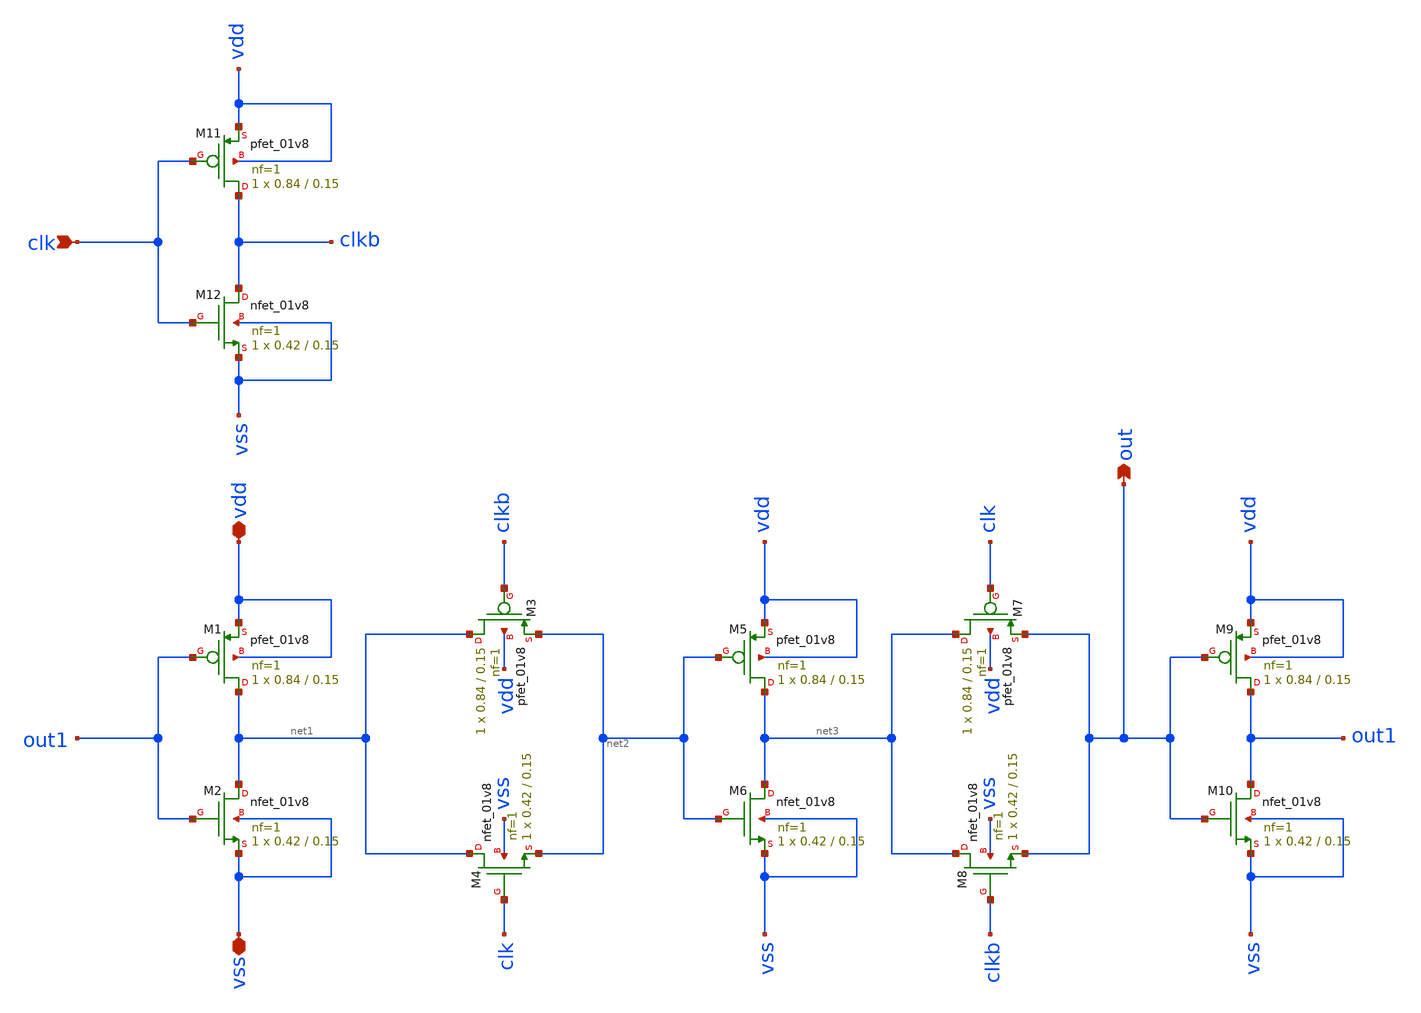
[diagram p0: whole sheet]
** sch_path: sch/PLL_caravel/FD.sch
**.subckt FD vss clk out vdd
*.iopin vss
*.ipin clk
*.opin out
*.iopin vdd
XM1 net1 out1 vdd vdd sky130_fd_pr__pfet_01v8 L=0.15 W=0.84 nf=1 ad='int((nf+1)/2) * W/nf * 0.29' as='int((nf+2)/2) * W/nf * 0.29'
+ pd='2*int((nf+1)/2) * (W/nf + 0.29)' ps='2*int((nf+2)/2) * (W/nf + 0.29)' nrd='0.29 / W' nrs='0.29 / W'
+ sa=0 sb=0 sd=0 mult=1 m=1
XM2 net1 out1 vss vss sky130_fd_pr__nfet_01v8 L=0.15 W=0.42 nf=1 ad='int((nf+1)/2) * W/nf * 0.29' as='int((nf+2)/2) * W/nf * 0.29'
+ pd='2*int((nf+1)/2) * (W/nf + 0.29)' ps='2*int((nf+2)/2) * (W/nf + 0.29)' nrd='0.29 / W' nrs='0.29 / W'
+ sa=0 sb=0 sd=0 mult=1 m=1
XM3 net1 clkb net2 vdd sky130_fd_pr__pfet_01v8 L=0.15 W=0.84 nf=1 ad='int((nf+1)/2) * W/nf * 0.29' as='int((nf+2)/2) * W/nf * 0.29'
+ pd='2*int((nf+1)/2) * (W/nf + 0.29)' ps='2*int((nf+2)/2) * (W/nf + 0.29)' nrd='0.29 / W' nrs='0.29 / W'
+ sa=0 sb=0 sd=0 mult=1 m=1
XM4 net1 clk net2 vss sky130_fd_pr__nfet_01v8 L=0.15 W=0.42 nf=1 ad='int((nf+1)/2) * W/nf * 0.29' as='int((nf+2)/2) * W/nf * 0.29'
+ pd='2*int((nf+1)/2) * (W/nf + 0.29)' ps='2*int((nf+2)/2) * (W/nf + 0.29)' nrd='0.29 / W' nrs='0.29 / W'
+ sa=0 sb=0 sd=0 mult=1 m=1
XM5 net3 net2 vdd vdd sky130_fd_pr__pfet_01v8 L=0.15 W=0.84 nf=1 ad='int((nf+1)/2) * W/nf * 0.29' as='int((nf+2)/2) * W/nf * 0.29'
+ pd='2*int((nf+1)/2) * (W/nf + 0.29)' ps='2*int((nf+2)/2) * (W/nf + 0.29)' nrd='0.29 / W' nrs='0.29 / W'
+ sa=0 sb=0 sd=0 mult=1 m=1
XM6 net3 net2 vss vss sky130_fd_pr__nfet_01v8 L=0.15 W=0.42 nf=1 ad='int((nf+1)/2) * W/nf * 0.29' as='int((nf+2)/2) * W/nf * 0.29'
+ pd='2*int((nf+1)/2) * (W/nf + 0.29)' ps='2*int((nf+2)/2) * (W/nf + 0.29)' nrd='0.29 / W' nrs='0.29 / W'
+ sa=0 sb=0 sd=0 mult=1 m=1
XM7 net3 clk out vdd sky130_fd_pr__pfet_01v8 L=0.15 W=0.84 nf=1 ad='int((nf+1)/2) * W/nf * 0.29' as='int((nf+2)/2) * W/nf * 0.29'
+ pd='2*int((nf+1)/2) * (W/nf + 0.29)' ps='2*int((nf+2)/2) * (W/nf + 0.29)' nrd='0.29 / W' nrs='0.29 / W'
+ sa=0 sb=0 sd=0 mult=1 m=1
XM8 net3 clkb out vss sky130_fd_pr__nfet_01v8 L=0.15 W=0.42 nf=1 ad='int((nf+1)/2) * W/nf * 0.29' as='int((nf+2)/2) * W/nf * 0.29'
+ pd='2*int((nf+1)/2) * (W/nf + 0.29)' ps='2*int((nf+2)/2) * (W/nf + 0.29)' nrd='0.29 / W' nrs='0.29 / W'
+ sa=0 sb=0 sd=0 mult=1 m=1
XM9 out1 out vdd vdd sky130_fd_pr__pfet_01v8 L=0.15 W=0.84 nf=1 ad='int((nf+1)/2) * W/nf * 0.29' as='int((nf+2)/2) * W/nf * 0.29'
+ pd='2*int((nf+1)/2) * (W/nf + 0.29)' ps='2*int((nf+2)/2) * (W/nf + 0.29)' nrd='0.29 / W' nrs='0.29 / W'
+ sa=0 sb=0 sd=0 mult=1 m=1
XM10 out1 out vss vss sky130_fd_pr__nfet_01v8 L=0.15 W=0.42 nf=1 ad='int((nf+1)/2) * W/nf * 0.29' as='int((nf+2)/2) * W/nf * 0.29'
+ pd='2*int((nf+1)/2) * (W/nf + 0.29)' ps='2*int((nf+2)/2) * (W/nf + 0.29)' nrd='0.29 / W' nrs='0.29 / W'
+ sa=0 sb=0 sd=0 mult=1 m=1
XM11 clkb clk vdd vdd sky130_fd_pr__pfet_01v8 L=0.15 W=0.84 nf=1 ad='int((nf+1)/2) * W/nf * 0.29' as='int((nf+2)/2) * W/nf * 0.29'
+ pd='2*int((nf+1)/2) * (W/nf + 0.29)' ps='2*int((nf+2)/2) * (W/nf + 0.29)' nrd='0.29 / W' nrs='0.29 / W'
+ sa=0 sb=0 sd=0 mult=1 m=1
XM12 clkb clk vss vss sky130_fd_pr__nfet_01v8 L=0.15 W=0.42 nf=1 ad='int((nf+1)/2) * W/nf * 0.29' as='int((nf+2)/2) * W/nf * 0.29'
+ pd='2*int((nf+1)/2) * (W/nf + 0.29)' ps='2*int((nf+2)/2) * (W/nf + 0.29)' nrd='0.29 / W' nrs='0.29 / W'
+ sa=0 sb=0 sd=0 mult=1 m=1
**.ends
.end
